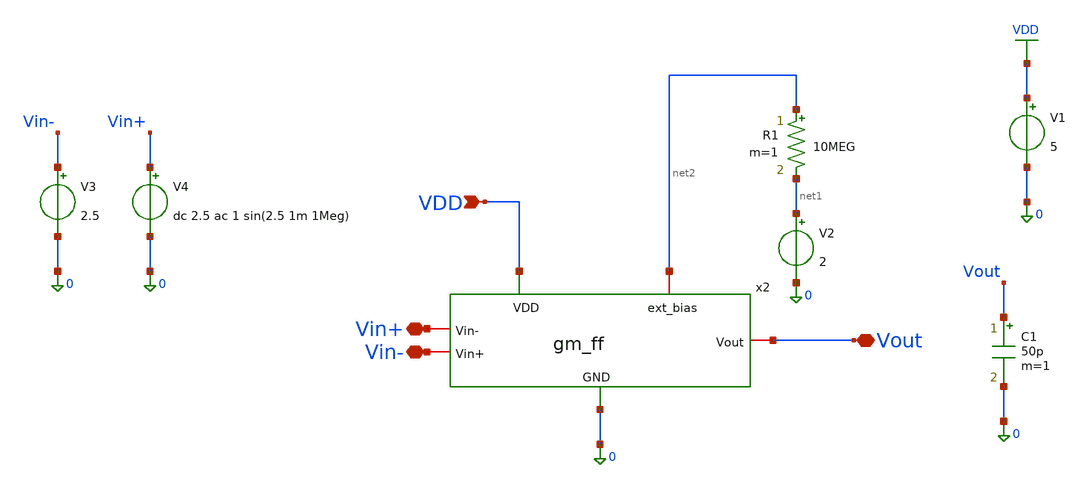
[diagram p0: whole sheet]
** sch_path: TG_gm_ff_testing/gm_ff_testing.sch
**.subckt gm_ff_testing VDD Vin- Vin+ Vout
*.ipin VDD
*.iopin Vin-
*.iopin Vin+
*.iopin Vout
V1 VDD 0 5
V3 Vin- 0 2.5
V4 Vin+ 0 dc 2.5 ac 1 sin(2.5 1m 1Meg)
R1 net2 net1 10MEG m=1
V2 net1 0 2
C1 Vout 0 50p m=1
x2 VDD Vout Vin+ Vin- net2 0 gm_ff
**** begin user architecture code



.include /foss/pdks/gf180mcuD/libs.tech/ngspice/design.ngspice
.lib /foss/pdks/gf180mcuD/libs.tech/ngspice/sm141064.ngspice typical
.lib /foss/pdks/gf180mcuD/libs.tech/ngspice/sm141064.ngspice res_typical

.control
  save all
  op
  print all
  print @m.xm2.m0[gm]
  print @m.xm2.m0[id]
  *show all
  ac dec 10 1 1G
  meas ac dc_gain MAX vdb(Vout)
  meas ac ugbw WHEN vdb(Vout)=0 FALL=1
  let phase_deg = (180/PI)*vp(Vout)
  plot vdb(Vout)
  plot phase_deg
.endc



**** end user architecture code
**.ends

* expanding   symbol:  TG_gm_ff_testing/gm_ff.sym # of pins=6
** sym_path: MRTMOS_final_chip/gm_ff.sym
** sch_path: MRTMOS_final_chip/gm_ff.sch
.subckt gm_ff VDD Vout Vin- Vin+ ext_bias GND
*.iopin ext_bias
*.ipin Vin+
*.ipin Vin-
*.iopin GND
*.iopin VDD
*.opin Vout
XC3 ext_bias GND cap_nmos_06v0 c_width=60e-6 c_length=10e-6 m=6
XC1 VDD GND cap_nmos_06v0 c_width=60e-6 c_length=10e-6 m=6
XM7 net2 ext_bias GND GND nfet_05v0 L=1.2u W=16u nf=8 ad='int((nf+1)/2) * W/nf * 0.18u' as='int((nf+2)/2) * W/nf * 0.18u'
+ pd='2*int((nf+1)/2) * (W/nf + 0.18u)' ps='2*int((nf+2)/2) * (W/nf + 0.18u)' nrd='0.18u / W' nrs='0.18u / W'
+ sa=0 sb=0 sd=0 m=2
XM8 Vout Vin- net2 GND nfet_05v0 L=1u W=7.5u nf=4 ad='int((nf+1)/2) * W/nf * 0.18u' as='int((nf+2)/2) * W/nf * 0.18u'
+ pd='2*int((nf+1)/2) * (W/nf + 0.18u)' ps='2*int((nf+2)/2) * (W/nf + 0.18u)' nrd='0.18u / W' nrs='0.18u / W'
+ sa=0 sb=0 sd=0 m=4
XM9 net1 net1 VDD VDD pfet_05v0 L=2u W=17u nf=10 ad='int((nf+1)/2) * W/nf * 0.18u' as='int((nf+2)/2) * W/nf * 0.18u'
+ pd='2*int((nf+1)/2) * (W/nf + 0.18u)' ps='2*int((nf+2)/2) * (W/nf + 0.18u)' nrd='0.18u / W' nrs='0.18u / W'
+ sa=0 sb=0 sd=0 m=2
XM5 ext_bias ext_bias GND GND nfet_05v0 L=1.2u W=16u nf=8 ad='int((nf+1)/2) * W/nf * 0.18u' as='int((nf+2)/2) * W/nf * 0.18u'
+ pd='2*int((nf+1)/2) * (W/nf + 0.18u)' ps='2*int((nf+2)/2) * (W/nf + 0.18u)' nrd='0.18u / W' nrs='0.18u / W'
+ sa=0 sb=0 sd=0 m=2
XM1 net1 Vin+ net2 GND nfet_05v0 L=1u W=7.5u nf=4 ad='int((nf+1)/2) * W/nf * 0.18u' as='int((nf+2)/2) * W/nf * 0.18u'
+ pd='2*int((nf+1)/2) * (W/nf + 0.18u)' ps='2*int((nf+2)/2) * (W/nf + 0.18u)' nrd='0.18u / W' nrs='0.18u / W'
+ sa=0 sb=0 sd=0 m=4
XM2 Vout net1 VDD VDD pfet_05v0 L=2u W=17u nf=10 ad='int((nf+1)/2) * W/nf * 0.18u' as='int((nf+2)/2) * W/nf * 0.18u'
+ pd='2*int((nf+1)/2) * (W/nf + 0.18u)' ps='2*int((nf+2)/2) * (W/nf + 0.18u)' nrd='0.18u / W' nrs='0.18u / W'
+ sa=0 sb=0 sd=0 m=2
.ends

.GLOBAL VDD
.end
